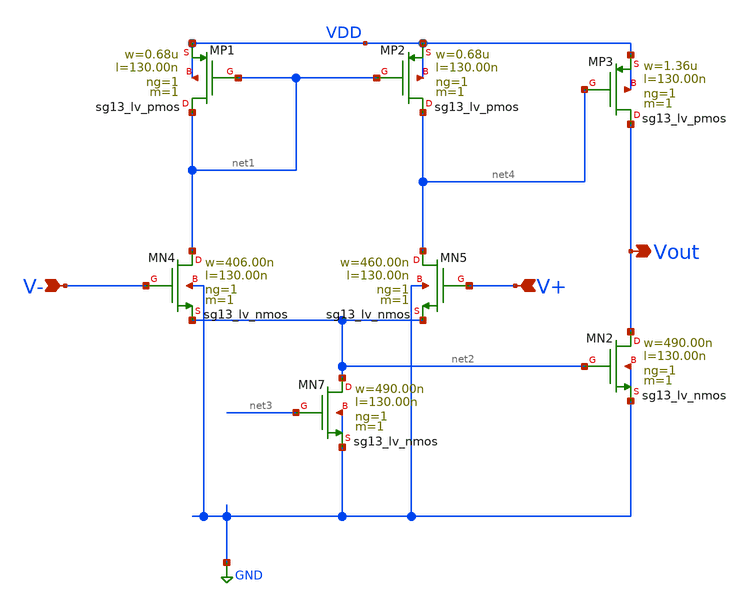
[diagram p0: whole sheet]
** sch_path: xschem/Opamp.sch
**.subckt Opamp V- V+ Vout
*.ipin V-
*.ipin V+
*.opin Vout
XMP1 net1 net1 VDD VDD sg13_lv_pmos w=0.68u l=130.00n ng=1 m=1 mm_ok=1
XMN4 net1 V- net2 GND sg13_lv_nmos w=406.00n l=130.00n ng=1 m=1 mm_ok=1
XMP2 net4 net1 VDD VDD sg13_lv_pmos w=0.68u l=130.00n ng=1 m=1 mm_ok=1
XMN5 net4 V+ net2 GND sg13_lv_nmos w=460.00n l=130.00n ng=1 m=1 mm_ok=1
XMN7 net2 net3 GND GND sg13_lv_nmos w=490.00n l=130.00n ng=1 m=1 mm_ok=1
XMN2 Vout net2 GND GND sg13_lv_nmos w=490.00n l=130.00n ng=1 m=1 mm_ok=1
XMP3 Vout net4 VDD VDD sg13_lv_pmos w=1.36u l=130.00n ng=1 m=1 mm_ok=1
**.ends
.GLOBAL GND
.end
